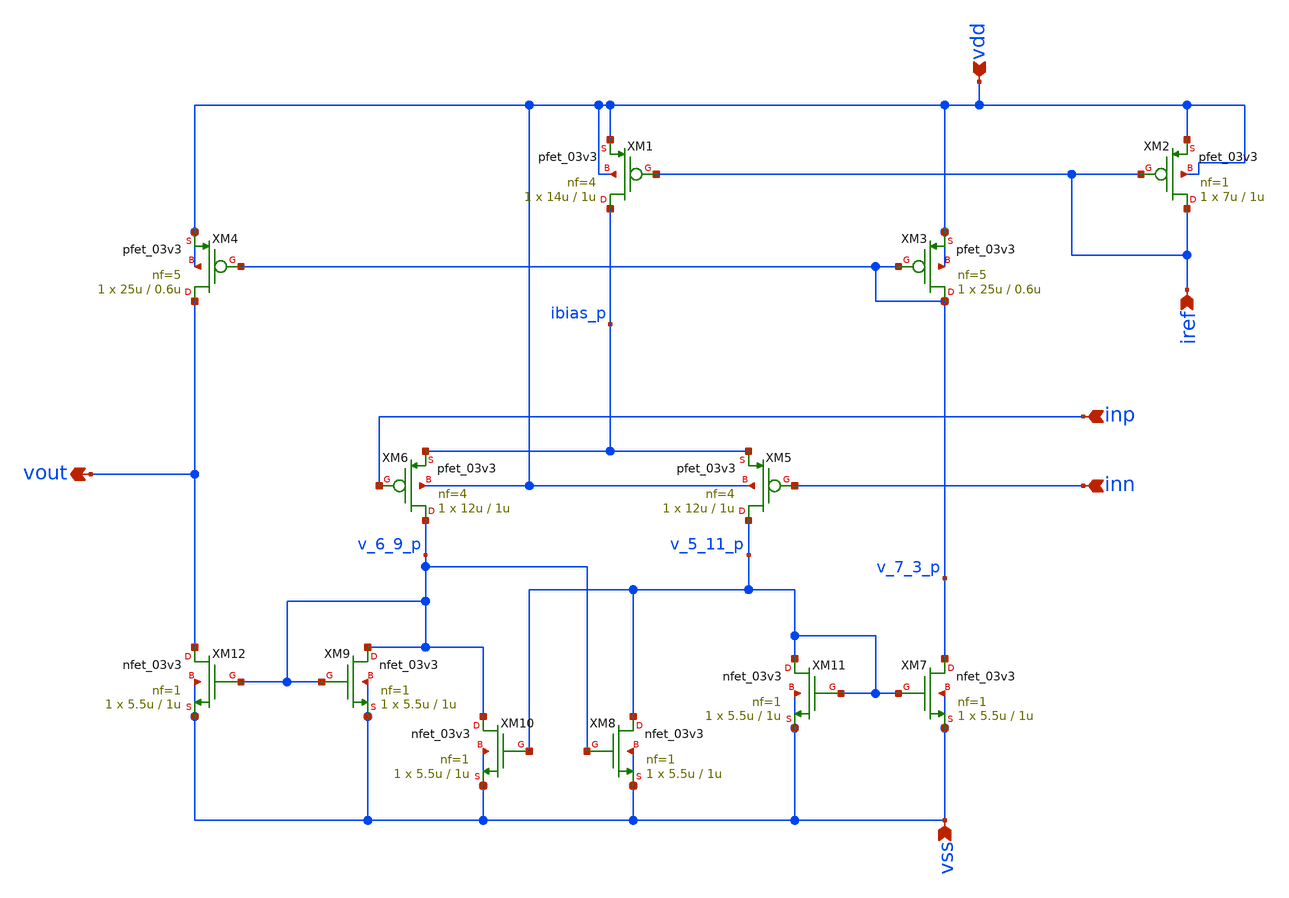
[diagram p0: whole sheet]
** sch_path: designs/libs/core_analog/Comparator/Pmos_Comparator.sch
**.subckt Pmos_Comparator vdd vss iref inn inp vout
*.ipin vdd
*.ipin vss
*.ipin iref
*.ipin inn
*.ipin inp
*.opin vout
XM3 v_7_3_p v_7_3_p vdd vdd pfet_03v3 L=0.6u W=25u nf=5 ad='int((nf+1)/2) * W/nf * 0.18u' as='int((nf+2)/2) * W/nf * 0.18u'
+ pd='2*int((nf+1)/2) * (W/nf + 0.18u)' ps='2*int((nf+2)/2) * (W/nf + 0.18u)' nrd='0.18u / W' nrs='0.18u / W'
+ sa=0 sb=0 sd=0 m=1
XM4 vout v_7_3_p vdd vdd pfet_03v3 L=0.6u W=25u nf=5 ad='int((nf+1)/2) * W/nf * 0.18u' as='int((nf+2)/2) * W/nf * 0.18u'
+ pd='2*int((nf+1)/2) * (W/nf + 0.18u)' ps='2*int((nf+2)/2) * (W/nf + 0.18u)' nrd='0.18u / W' nrs='0.18u / W'
+ sa=0 sb=0 sd=0 m=1
XM5 v_5_11_p inn ibias_p vdd pfet_03v3 L=1u W=12u nf=4 ad='int((nf+1)/2) * W/nf * 0.18u' as='int((nf+2)/2) * W/nf * 0.18u'
+ pd='2*int((nf+1)/2) * (W/nf + 0.18u)' ps='2*int((nf+2)/2) * (W/nf + 0.18u)' nrd='0.18u / W' nrs='0.18u / W'
+ sa=0 sb=0 sd=0 m=1
XM6 v_6_9_p inp ibias_p vdd pfet_03v3 L=1u W=12u nf=4 ad='int((nf+1)/2) * W/nf * 0.18u' as='int((nf+2)/2) * W/nf * 0.18u'
+ pd='2*int((nf+1)/2) * (W/nf + 0.18u)' ps='2*int((nf+2)/2) * (W/nf + 0.18u)' nrd='0.18u / W' nrs='0.18u / W'
+ sa=0 sb=0 sd=0 m=1
XM7 v_7_3_p v_5_11_p vss vss nfet_03v3 L=1u W=5.5u nf=1 ad='int((nf+1)/2) * W/nf * 0.18u' as='int((nf+2)/2) * W/nf * 0.18u'
+ pd='2*int((nf+1)/2) * (W/nf + 0.18u)' ps='2*int((nf+2)/2) * (W/nf + 0.18u)' nrd='0.18u / W' nrs='0.18u / W'
+ sa=0 sb=0 sd=0 m=1
XM8 v_5_11_p v_6_9_p vss vss nfet_03v3 L=1u W=5.5u nf=1 ad='int((nf+1)/2) * W/nf * 0.18u' as='int((nf+2)/2) * W/nf * 0.18u'
+ pd='2*int((nf+1)/2) * (W/nf + 0.18u)' ps='2*int((nf+2)/2) * (W/nf + 0.18u)' nrd='0.18u / W' nrs='0.18u / W'
+ sa=0 sb=0 sd=0 m=1
XM9 v_6_9_p v_6_9_p vss vss nfet_03v3 L=1u W=5.5u nf=1 ad='int((nf+1)/2) * W/nf * 0.18u' as='int((nf+2)/2) * W/nf * 0.18u'
+ pd='2*int((nf+1)/2) * (W/nf + 0.18u)' ps='2*int((nf+2)/2) * (W/nf + 0.18u)' nrd='0.18u / W' nrs='0.18u / W'
+ sa=0 sb=0 sd=0 m=1
XM10 v_6_9_p v_5_11_p vss vss nfet_03v3 L=1u W=5.5u nf=1 ad='int((nf+1)/2) * W/nf * 0.18u' as='int((nf+2)/2) * W/nf * 0.18u'
+ pd='2*int((nf+1)/2) * (W/nf + 0.18u)' ps='2*int((nf+2)/2) * (W/nf + 0.18u)' nrd='0.18u / W' nrs='0.18u / W'
+ sa=0 sb=0 sd=0 m=1
XM11 v_5_11_p v_5_11_p vss vss nfet_03v3 L=1u W=5.5u nf=1 ad='int((nf+1)/2) * W/nf * 0.18u' as='int((nf+2)/2) * W/nf * 0.18u'
+ pd='2*int((nf+1)/2) * (W/nf + 0.18u)' ps='2*int((nf+2)/2) * (W/nf + 0.18u)' nrd='0.18u / W' nrs='0.18u / W'
+ sa=0 sb=0 sd=0 m=1
XM12 vout v_6_9_p vss vss nfet_03v3 L=1u W=5.5u nf=1 ad='int((nf+1)/2) * W/nf * 0.18u' as='int((nf+2)/2) * W/nf * 0.18u'
+ pd='2*int((nf+1)/2) * (W/nf + 0.18u)' ps='2*int((nf+2)/2) * (W/nf + 0.18u)' nrd='0.18u / W' nrs='0.18u / W'
+ sa=0 sb=0 sd=0 m=1
XM1 ibias_p iref vdd vdd pfet_03v3 L=1u W=14u nf=4 ad='int((nf+1)/2) * W/nf * 0.18u' as='int((nf+2)/2) * W/nf * 0.18u'
+ pd='2*int((nf+1)/2) * (W/nf + 0.18u)' ps='2*int((nf+2)/2) * (W/nf + 0.18u)' nrd='0.18u / W' nrs='0.18u / W'
+ sa=0 sb=0 sd=0 m=1
XM2 iref iref vdd vdd pfet_03v3 L=1u W=7u nf=1 ad='int((nf+1)/2) * W/nf * 0.18u' as='int((nf+2)/2) * W/nf * 0.18u'
+ pd='2*int((nf+1)/2) * (W/nf + 0.18u)' ps='2*int((nf+2)/2) * (W/nf + 0.18u)' nrd='0.18u / W' nrs='0.18u / W'
+ sa=0 sb=0 sd=0 m=1
**.ends
.end
